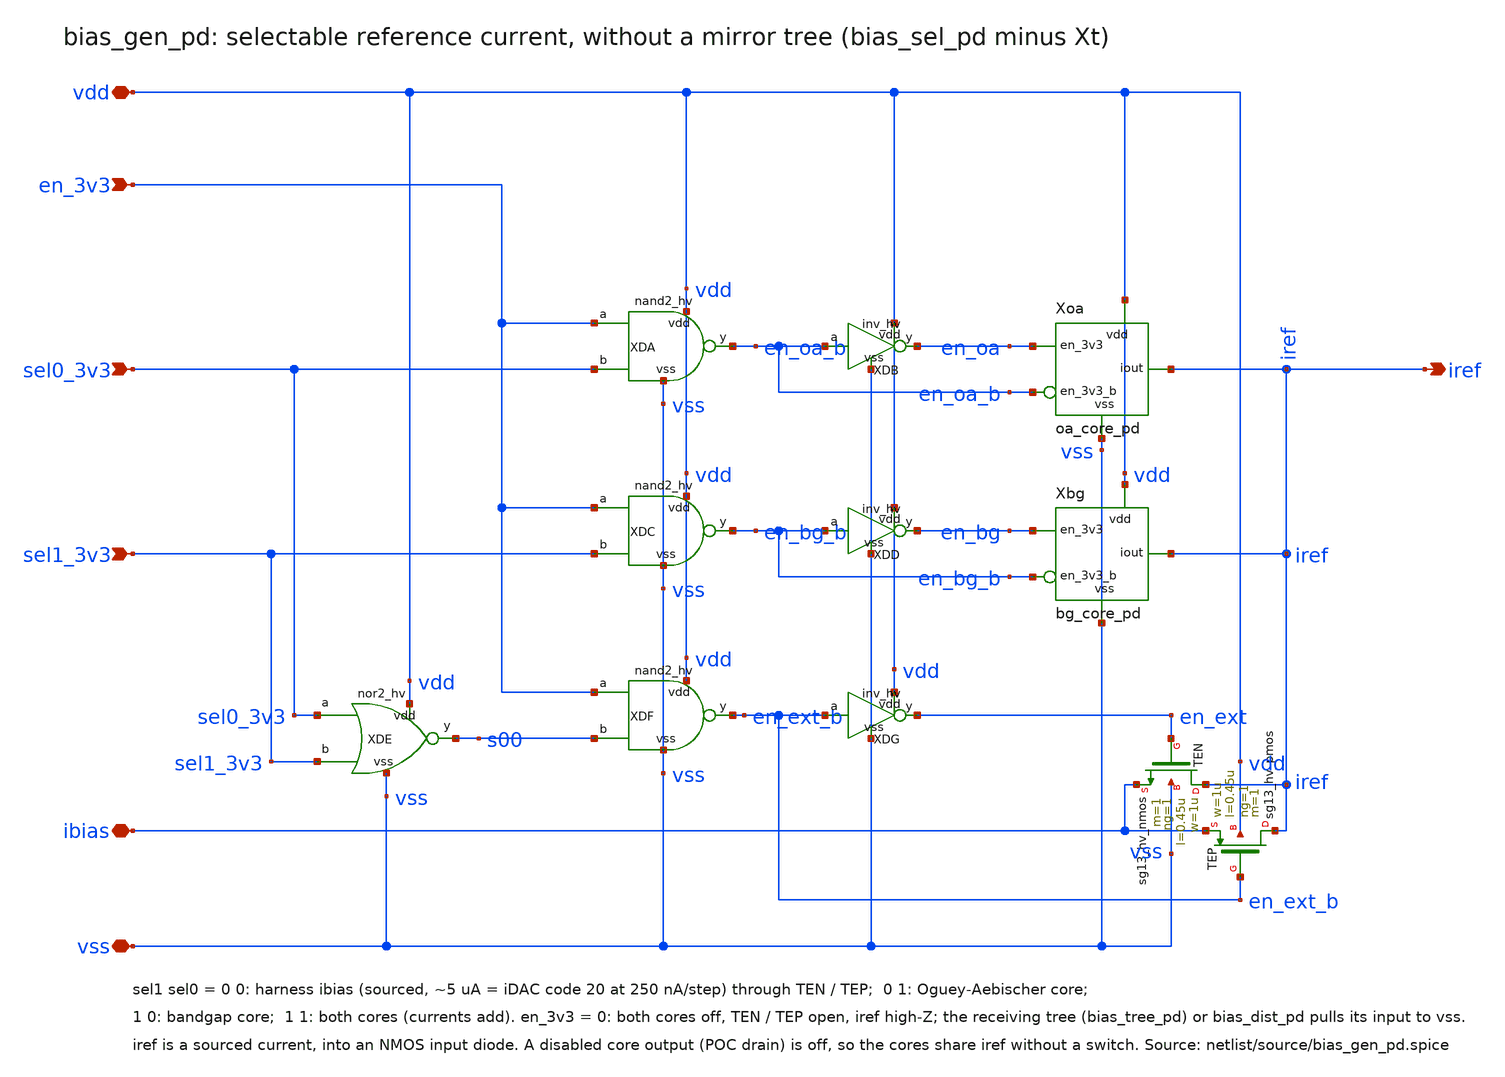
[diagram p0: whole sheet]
** sch_path: macros/bias_gen_pd/schematic/xschem/bias_gen_pd.sch
**.subckt bias_gen_pd vdd vss ibias iref en_3v3 sel0_3v3 sel1_3v3
*.iopin vdd
*.iopin vss
*.iopin ibias
*.opin iref
*.ipin en_3v3
*.ipin sel0_3v3
*.ipin sel1_3v3
XDA vdd vss en_3v3 sel0_3v3 en_oa_b nand2_hv
XDB vdd vss en_oa_b en_oa inv_hv
XDC vdd vss en_3v3 sel1_3v3 en_bg_b nand2_hv
XDD vdd vss en_bg_b en_bg inv_hv
XDE vdd vss sel0_3v3 sel1_3v3 s00 nor2_hv
XDF vdd vss en_3v3 s00 en_ext_b nand2_hv
XDG vdd vss en_ext_b en_ext inv_hv
Xoa vdd vss iref en_oa en_oa_b oa_core_pd
Xbg vdd vss iref en_bg en_bg_b bg_core_pd
XTEN iref en_ext ibias vss sg13_hv_nmos w=1u l=0.45u ng=1 m=1 mm_ok=1
XTEP iref en_ext_b ibias vdd sg13_hv_pmos w=1u l=0.45u ng=1 m=1 mm_ok=1
**.ends
.end
